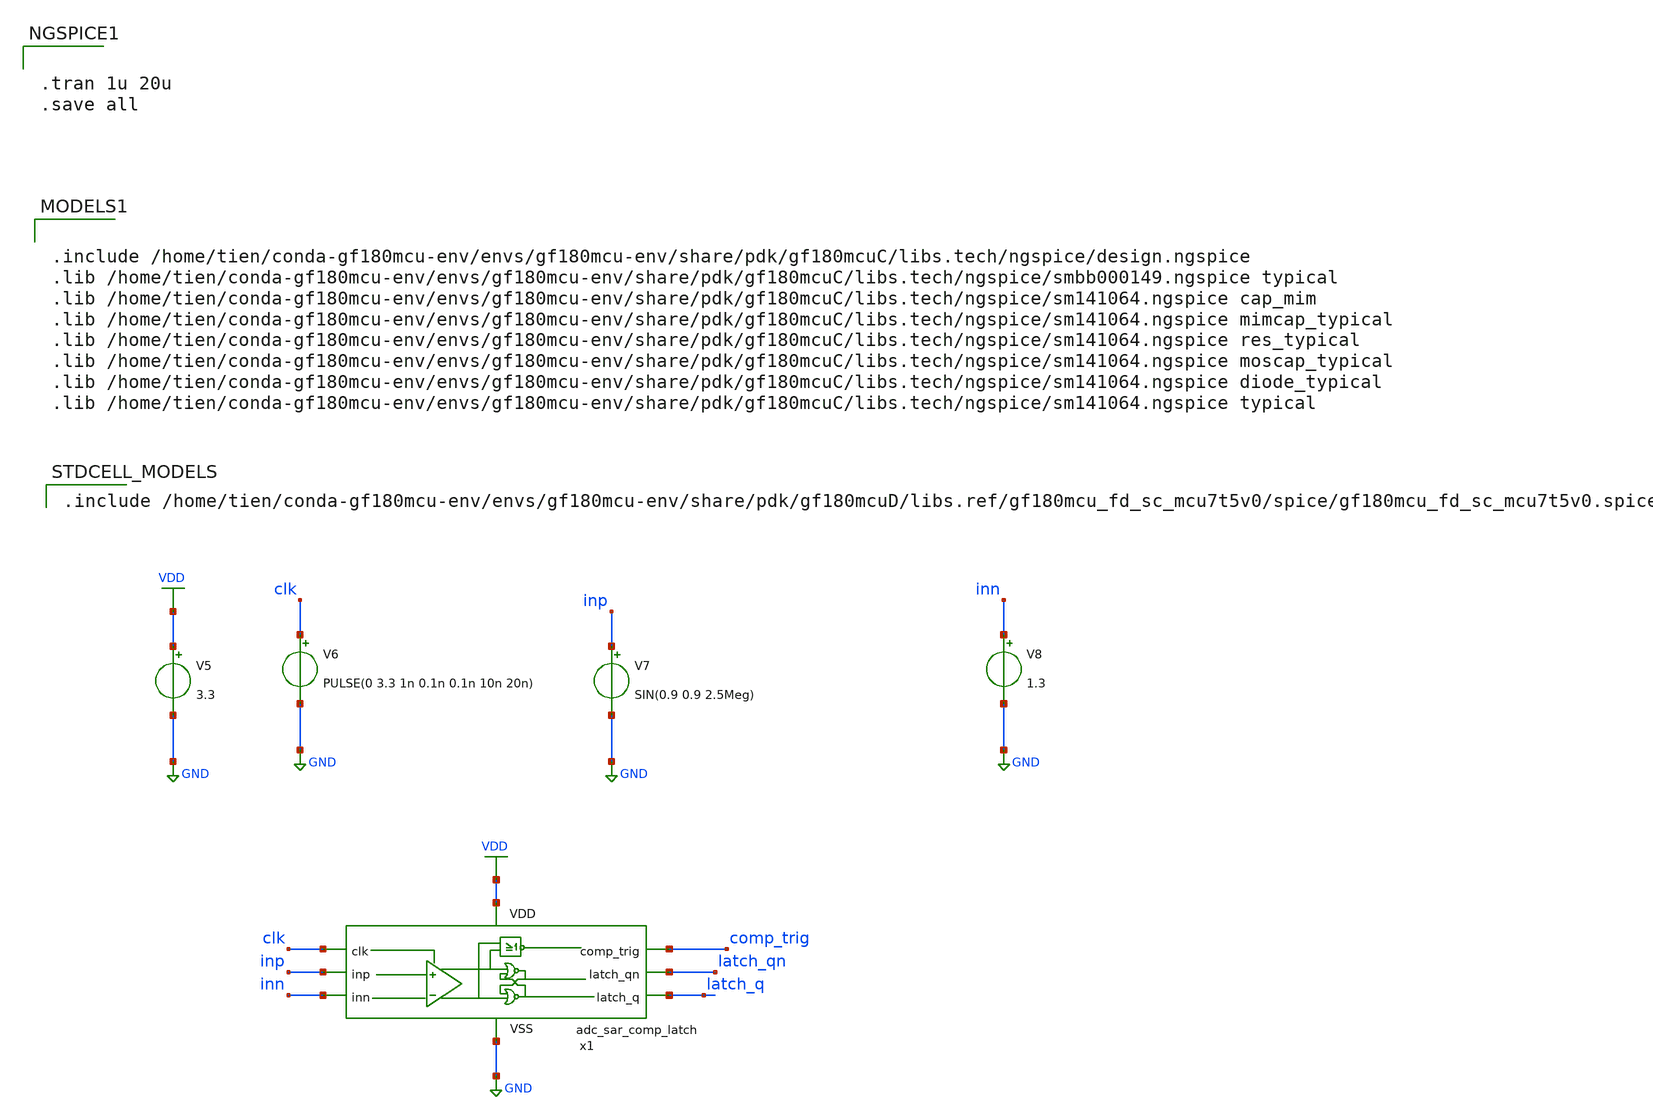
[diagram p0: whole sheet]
** sch_path: spice/adc_sar_comp_latch_tb2.sch
**.subckt adc_sar_comp_latch_tb2
V5 VDD GND 3.3
V6 clk GND PULSE(0 3.3 1n 0.1n 0.1n 10n 20n)
V7 inp GND SIN(0.9 0.9 2.5Meg)
V8 inn GND 1.3
x1 VDD GND clk inp inn comp_trig latch_qn latch_q adc_sar_comp_latch
**** begin user architecture code


.tran 1u 20u
.save all



.include /home/tien/conda-gf180mcu-env/envs/gf180mcu-env/share/pdk/gf180mcuC/libs.tech/ngspice/design.ngspice
.lib /home/tien/conda-gf180mcu-env/envs/gf180mcu-env/share/pdk/gf180mcuC/libs.tech/ngspice/smbb000149.ngspice typical
.lib /home/tien/conda-gf180mcu-env/envs/gf180mcu-env/share/pdk/gf180mcuC/libs.tech/ngspice/sm141064.ngspice cap_mim
.lib /home/tien/conda-gf180mcu-env/envs/gf180mcu-env/share/pdk/gf180mcuC/libs.tech/ngspice/sm141064.ngspice mimcap_typical
.lib /home/tien/conda-gf180mcu-env/envs/gf180mcu-env/share/pdk/gf180mcuC/libs.tech/ngspice/sm141064.ngspice res_typical
.lib /home/tien/conda-gf180mcu-env/envs/gf180mcu-env/share/pdk/gf180mcuC/libs.tech/ngspice/sm141064.ngspice moscap_typical
.lib /home/tien/conda-gf180mcu-env/envs/gf180mcu-env/share/pdk/gf180mcuC/libs.tech/ngspice/sm141064.ngspice diode_typical
.lib /home/tien/conda-gf180mcu-env/envs/gf180mcu-env/share/pdk/gf180mcuC/libs.tech/ngspice/sm141064.ngspice typical

 .include /home/tien/conda-gf180mcu-env/envs/gf180mcu-env/share/pdk/gf180mcuD/libs.ref/gf180mcu_fd_sc_mcu7t5v0/spice/gf180mcu_fd_sc_mcu7t5v0.spice
**** end user architecture code
**.ends
.GLOBAL GND
.GLOBAL VDD
.end
